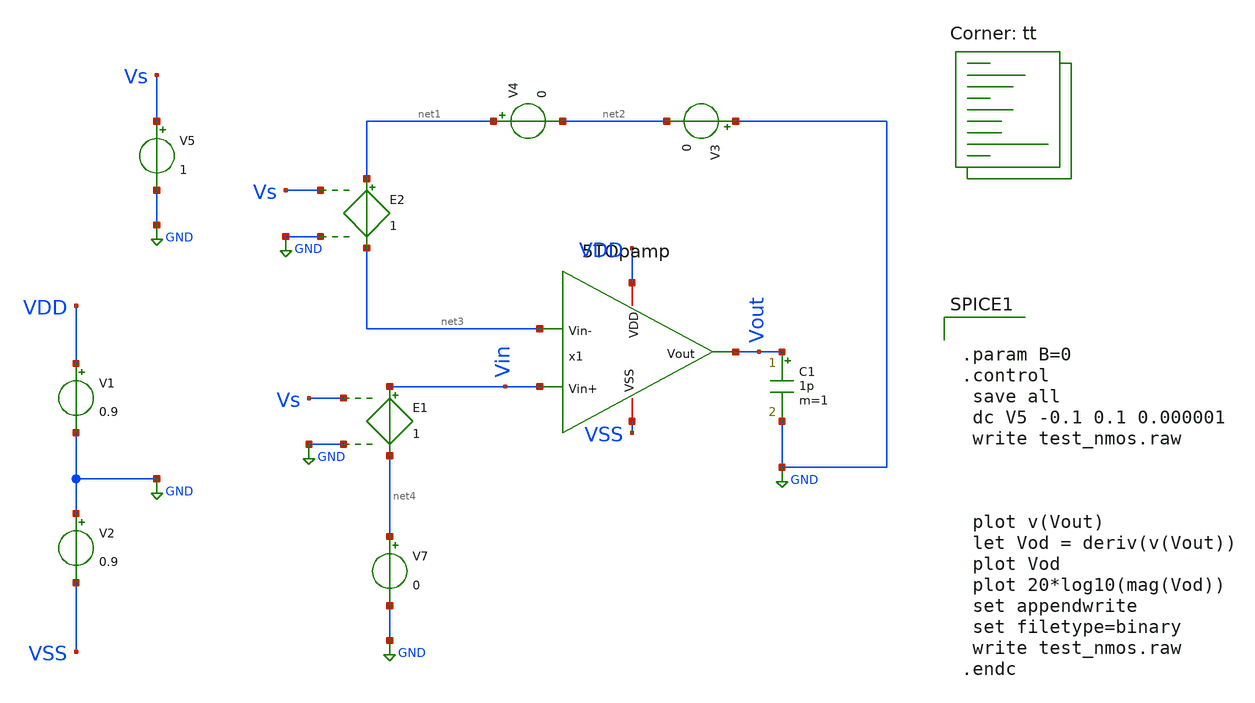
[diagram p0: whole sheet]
** sch_path: xschem/TestBenches/DCtestbench.sch
**.subckt DCtestbench
V1 VDD GND 0.9
V2 GND VSS 0.9
x1 VDD Vout net3 Vin VSS 5TOpamp
C1 Vout GND 1p m=1
V3 GND net2 0
V4 net1 net2 0
V7 net4 GND 0
E1 Vin net4 Vs GND 1
E2 net1 net3 Vs GND 1
V5 Vs GND 1
**** begin user architecture code
.lib $::SKYWATER_MODELS/sky130.lib.spice tt


.param B=0
.control
 save all
 dc V5 -0.1 0.1 0.000001
 write test_nmos.raw



 plot v(Vout)
 let Vod = deriv(v(Vout))
 plot Vod
 plot 20*log10(mag(Vod))
 set appendwrite
 set filetype=binary
 write test_nmos.raw
.endc


**** end user architecture code
**.ends

* expanding   symbol:  Amplifiers/5TOpamp.sym # of pins=5
** sym_path: xschem/Amplifiers/5TOpamp.sym
** sch_path: xschem/Amplifiers/5TOpamp.sch
.subckt 5TOpamp VDD Vout Vin- Vin+ VSS
*.iopin VDD
*.iopin VSS
*.ipin Vin-
*.ipin Vin+
*.opin Vout
I0 VDD Vb1 50u
XM1 Vcm Vin+ Vsink VSS sky130_fd_pr__nfet_01v8 L=0.75 W=4 nf=1 ad='int((nf+1)/2) * W/nf * 0.29' as='int((nf+2)/2) * W/nf * 0.29'
+ pd='2*int((nf+1)/2) * (W/nf + 0.29)' ps='2*int((nf+2)/2) * (W/nf + 0.29)' nrd='0.29 / W' nrs='0.29 / W'
+ sa=0 sb=0 sd=0 mult=3 m=3
XM2 Vout Vin- Vsink VSS sky130_fd_pr__nfet_01v8 L=0.75 W=4 nf=1 ad='int((nf+1)/2) * W/nf * 0.29' as='int((nf+2)/2) * W/nf * 0.29'
+ pd='2*int((nf+1)/2) * (W/nf + 0.29)' ps='2*int((nf+2)/2) * (W/nf + 0.29)' nrd='0.29 / W' nrs='0.29 / W'
+ sa=0 sb=0 sd=0 mult=3 m=3
XM3 Vb1 Vb1 VSS VSS sky130_fd_pr__nfet_01v8 L=0.75 W=5 nf=1 ad='int((nf+1)/2) * W/nf * 0.29' as='int((nf+2)/2) * W/nf * 0.29'
+ pd='2*int((nf+1)/2) * (W/nf + 0.29)' ps='2*int((nf+2)/2) * (W/nf + 0.29)' nrd='0.29 / W' nrs='0.29 / W'
+ sa=0 sb=0 sd=0 mult=1 m=1
XM4 Vsink Vb1 VSS VSS sky130_fd_pr__nfet_01v8 L=0.75 W=5 nf=1 ad='int((nf+1)/2) * W/nf * 0.29' as='int((nf+2)/2) * W/nf * 0.29'
+ pd='2*int((nf+1)/2) * (W/nf + 0.29)' ps='2*int((nf+2)/2) * (W/nf + 0.29)' nrd='0.29 / W' nrs='0.29 / W'
+ sa=0 sb=0 sd=0 mult=4 m=4
XM5 Vcm Vcm VDD VDD sky130_fd_pr__pfet_01v8_lvt L=0.75 W=10 nf=1 ad='int((nf+1)/2) * W/nf * 0.29' as='int((nf+2)/2) * W/nf * 0.29'
+ pd='2*int((nf+1)/2) * (W/nf + 0.29)' ps='2*int((nf+2)/2) * (W/nf + 0.29)' nrd='0.29 / W' nrs='0.29 / W'
+ sa=0 sb=0 sd=0 mult=1 m=1
XM6 Vout Vcm VDD VDD sky130_fd_pr__pfet_01v8_lvt L=0.75 W=10 nf=1 ad='int((nf+1)/2) * W/nf * 0.29' as='int((nf+2)/2) * W/nf * 0.29'
+ pd='2*int((nf+1)/2) * (W/nf + 0.29)' ps='2*int((nf+2)/2) * (W/nf + 0.29)' nrd='0.29 / W' nrs='0.29 / W'
+ sa=0 sb=0 sd=0 mult=1 m=1
.ends

.GLOBAL GND
.end
